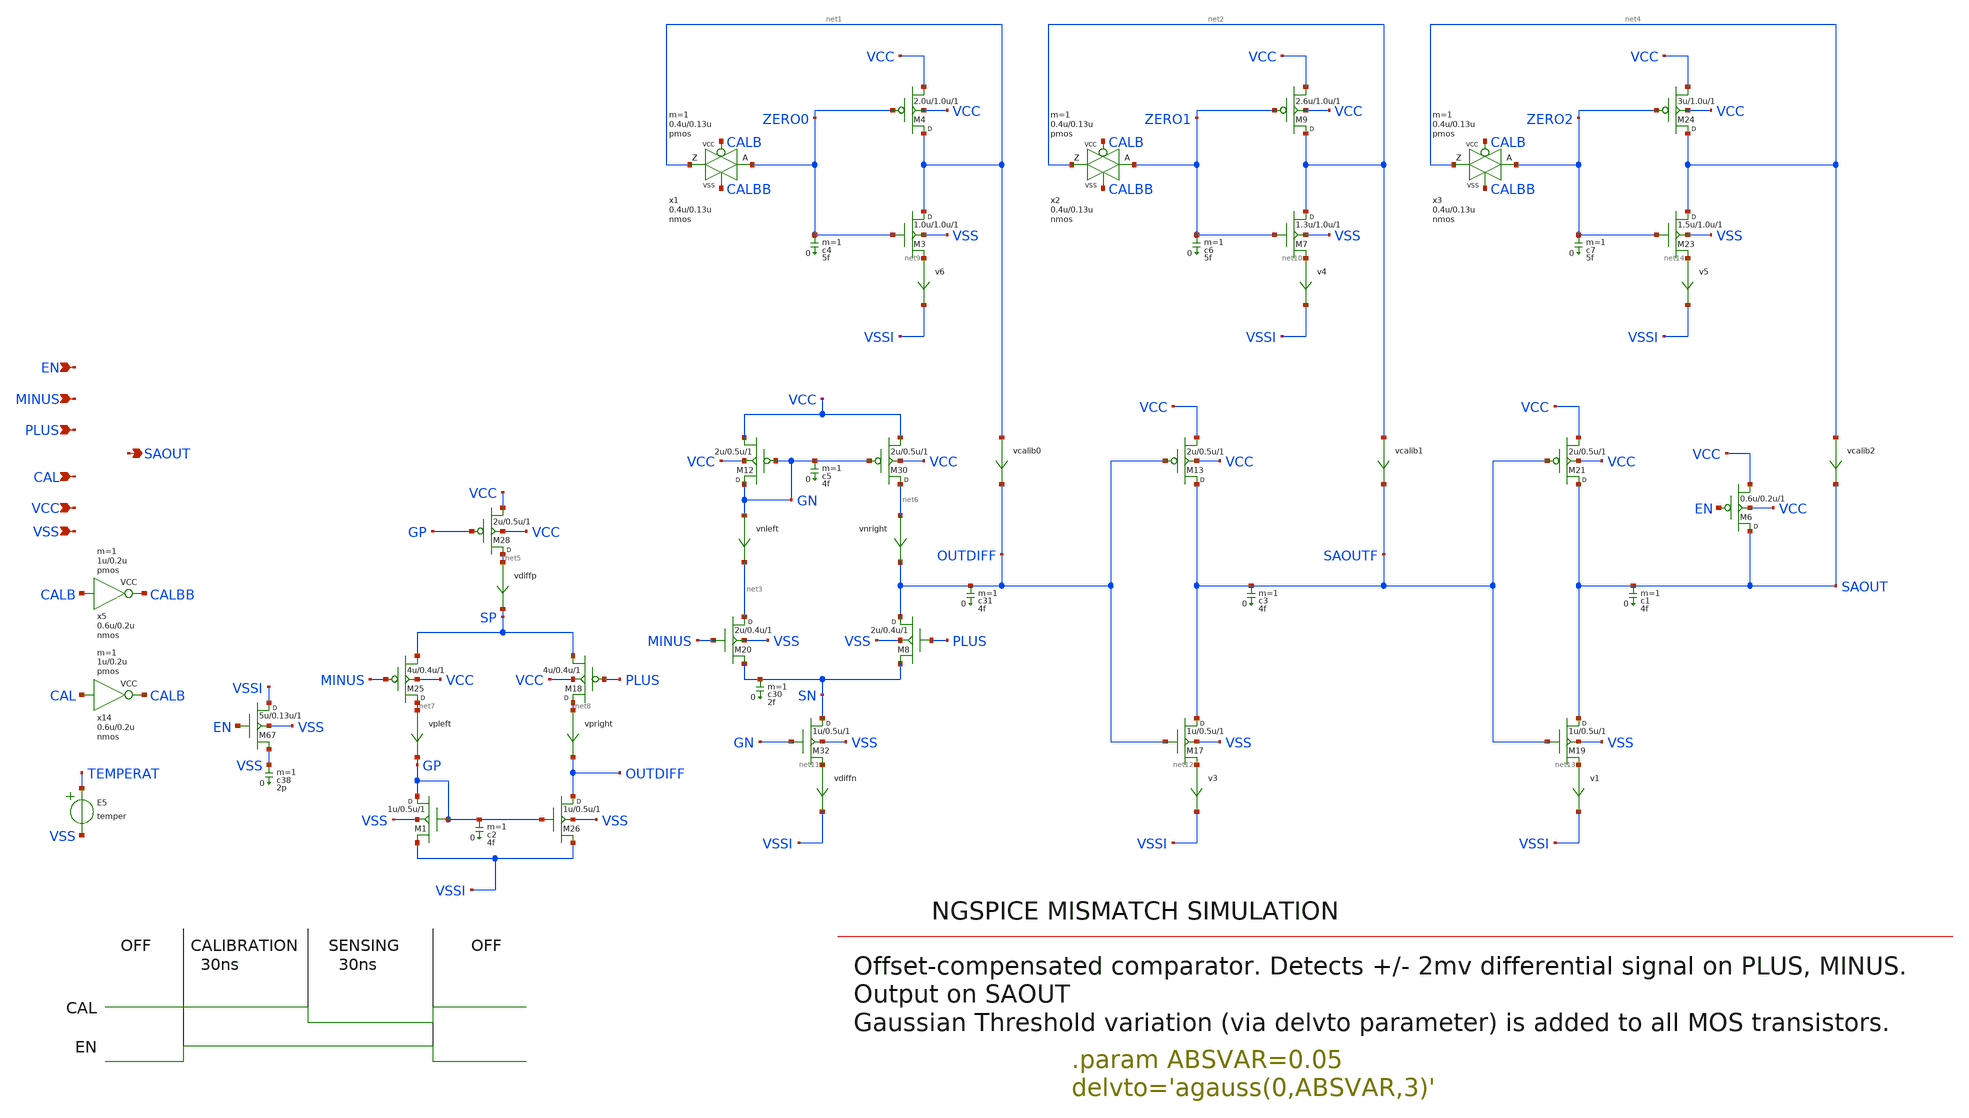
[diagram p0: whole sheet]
** sch_path: xschem-src/xschem_library/ngspice/autozero_comp.sch
* Copyright (C) 1998-2026 Stefan Frederik Schippers
* This program is free software; you can redistribute it and/or modify
* it under the terms of the GNU General Public License as published by
* the Free Software Foundation; either version 2 of the License, or
* (at your option) any later version.
* This program is distributed in the hope that it will be useful,
* but WITHOUT ANY WARRANTY; without even the implied warranty of
* MERCHANTABILITY or FITNESS FOR A PARTICULAR PURPOSE.  See the
* GNU General Public License for more details.
* You should have received a copy of the GNU General Public License
* along with this program; if not, write to the Free Software
**.subckt autozero_comp CAL PLUS MINUS EN VSS VCC SAOUT
*.ipin CAL
*.ipin PLUS
*.ipin MINUS
*.ipin EN
*.ipin VSS
*.ipin VCC
*.opin SAOUT
E5 TEMPERAT VSS VOL=' temper '
MAx14 CALB CAL VCC VCC pmos w=1u l=0.2u m=1
MBx14 CALB CAL VSS VSS nmos w=0.6u l=0.2u m=1
MAx5 CALBB CALB VCC VCC pmos w=1u l=0.2u m=1
MBx5 CALBB CALB VSS VSS nmos w=0.6u l=0.2u m=1
M67 VSSI EN VSS VSS nmos w=5u l=0.13u delvto='agauss(0,ABSVAR,3)' m=1
c38 VSS 0 2p m=1
MAx1 net1 CALB ZERO0 VCC pmos w=0.4u l=0.13u delvto='agauss(0,ABSVAR,3)' m=1
MBx1 net1 CALBB ZERO0 VSS nmos w=0.4u l=0.13u m=1
M3 net1 ZERO0 net9 VSS nmos w=1.0u l=1.0u delvto='agauss(0,ABSVAR,3)' m=1
M4 net1 ZERO0 VCC VCC pmos w=2.0u l=1.0u delvto='agauss(0,ABSVAR,3)' m=1
MAx2 net2 CALB ZERO1 VCC pmos w=0.4u l=0.13u delvto='agauss(0,ABSVAR,3)' m=1
MBx2 net2 CALBB ZERO1 VSS nmos w=0.4u l=0.13u m=1
M7 net2 ZERO1 net10 VSS nmos w=1.3u l=1.0u delvto='agauss(0,ABSVAR,3)' m=1
M9 net2 ZERO1 VCC VCC pmos w=2.6u l=1.0u delvto='agauss(0,ABSVAR,3)' m=1
M20 net3 MINUS SN VSS nmos w=2u l=0.4u delvto='agauss(0,ABSVAR,3)' m=1
M8 OUTDIFF PLUS SN VSS nmos w=2u l=0.4u delvto='agauss(0,ABSVAR,3)' m=1
M30 net6 GN VCC VCC pmos w=2u l=0.5u delvto='agauss(0,ABSVAR,3)' m=1
M12 GN GN VCC VCC pmos w=2u l=0.5u delvto='agauss(0,ABSVAR,3)' m=1
M32 SN GN net11 VSS nmos w=1u l=0.5u delvto='agauss(0,ABSVAR,3)' m=1
M17 SAOUTF OUTDIFF net12 VSS nmos w=1u l=0.5u delvto='agauss(0,ABSVAR,3)' m=1
M13 SAOUTF OUTDIFF VCC VCC pmos w=2u l=0.5u delvto='agauss(0,ABSVAR,3)' m=1
c3 SAOUTF 0 4f m=1
c5 GN 0 4f m=1
c30 SN 0 2f m=1
c31 OUTDIFF 0 4f m=1
vdiffn net11 VSSI 0
.save i(vdiffn)
v3 net12 VSSI 0
.save i(v3)
v4 net10 VSSI 0
.save i(v4)
v6 net9 VSSI 0
.save i(v6)
M19 SAOUT SAOUTF net13 VSS nmos w=1u l=0.5u delvto='agauss(0,ABSVAR,3)' m=1
M21 SAOUT SAOUTF VCC VCC pmos w=2u l=0.5u delvto='agauss(0,ABSVAR,3)' m=1
c1 SAOUT 0 4f m=1
v1 net13 VSSI 0
.save i(v1)
MAx3 net4 CALB ZERO2 VCC pmos w=0.4u l=0.13u delvto='agauss(0,ABSVAR,3)' m=1
MBx3 net4 CALBB ZERO2 VSS nmos w=0.4u l=0.13u m=1
M23 net4 ZERO2 net14 VSS nmos w=1.5u l=1.0u delvto='agauss(0,ABSVAR,3)' m=1
M24 net4 ZERO2 VCC VCC pmos w=3u l=1.0u delvto='agauss(0,ABSVAR,3)' m=1
v5 net14 VSSI 0
.save i(v5)
M6 SAOUT EN VCC VCC pmos w=0.6u l=0.2u delvto='agauss(0,ABSVAR,3)' m=1
M18 net8 PLUS SP VCC pmos w=4u l=0.4u delvto='agauss(0,ABSVAR,3)' m=1
M25 net7 MINUS SP VCC pmos w=4u l=0.4u delvto='agauss(0,ABSVAR,3)' m=1
M28 net5 GP VCC VCC pmos w=2u l=0.5u delvto='agauss(0,ABSVAR,3)' m=1
M26 OUTDIFF GP VSSI VSS nmos w=1u l=0.5u delvto='agauss(0,ABSVAR,3)' m=1
M1 GP GP VSSI VSS nmos w=1u l=0.5u delvto='agauss(0,ABSVAR,3)' m=1
c2 GP 0 4f m=1
c4 ZERO0 0 5f m=1
c6 ZERO1 0 5f m=1
c7 ZERO2 0 5f m=1
vdiffp net5 SP 0
.save i(vdiffp)
vcalib0 net1 OUTDIFF 0
.save i(vcalib0)
vcalib1 net2 SAOUTF 0
.save i(vcalib1)
vcalib2 net4 SAOUT 0
.save i(vcalib2)
vnleft GN net3 0
.save i(vnleft)
vnright net6 OUTDIFF 0
.save i(vnright)
vpleft net7 GP 0
.save i(vpleft)
vpright net8 OUTDIFF 0
.save i(vpright)
**** begin user architecture code

* .option SCALE=1e-6
.option method=gear
.param VCC=0.9
.param VDL='VCC/2+0.2'
.param ABSVAR=0.05
.temp 25
.param RNDVAL = 'agauss(0, 10, 1)'
** to generate following file:
** copy .../share/doc/xschem/ngspice/stimuli.autozero_comp to simulation directory
** then do 'Simulation->Utile Stimuli Editor (GUI)' and press 'Translate'
.include "stimuli_autozero_comp.cir"

** download models from here:
** http://ptm.asu.edu/modelcard/2006/130nm_bulk.pm
** and save to 'models_autozero_comp.txt' in simulation directory
.include "models_autozero_comp.txt"


* .tran 0.1n 900n uic

.control
  * setseed 17
  * reset
  * echo Seed=$rndseed
  let run=1
  dowhile run <= 300
    if run > 1
      set appendwrite
      reset
    end
    * save saout cal i(vvcc) en plus minus saoutf outdiff
    save all
    tran 0.5n 900n uic
    write autozero_comp.raw
    let run = run + 1
  end
  quit 0
.endc


**** end user architecture code
**.ends
.end
